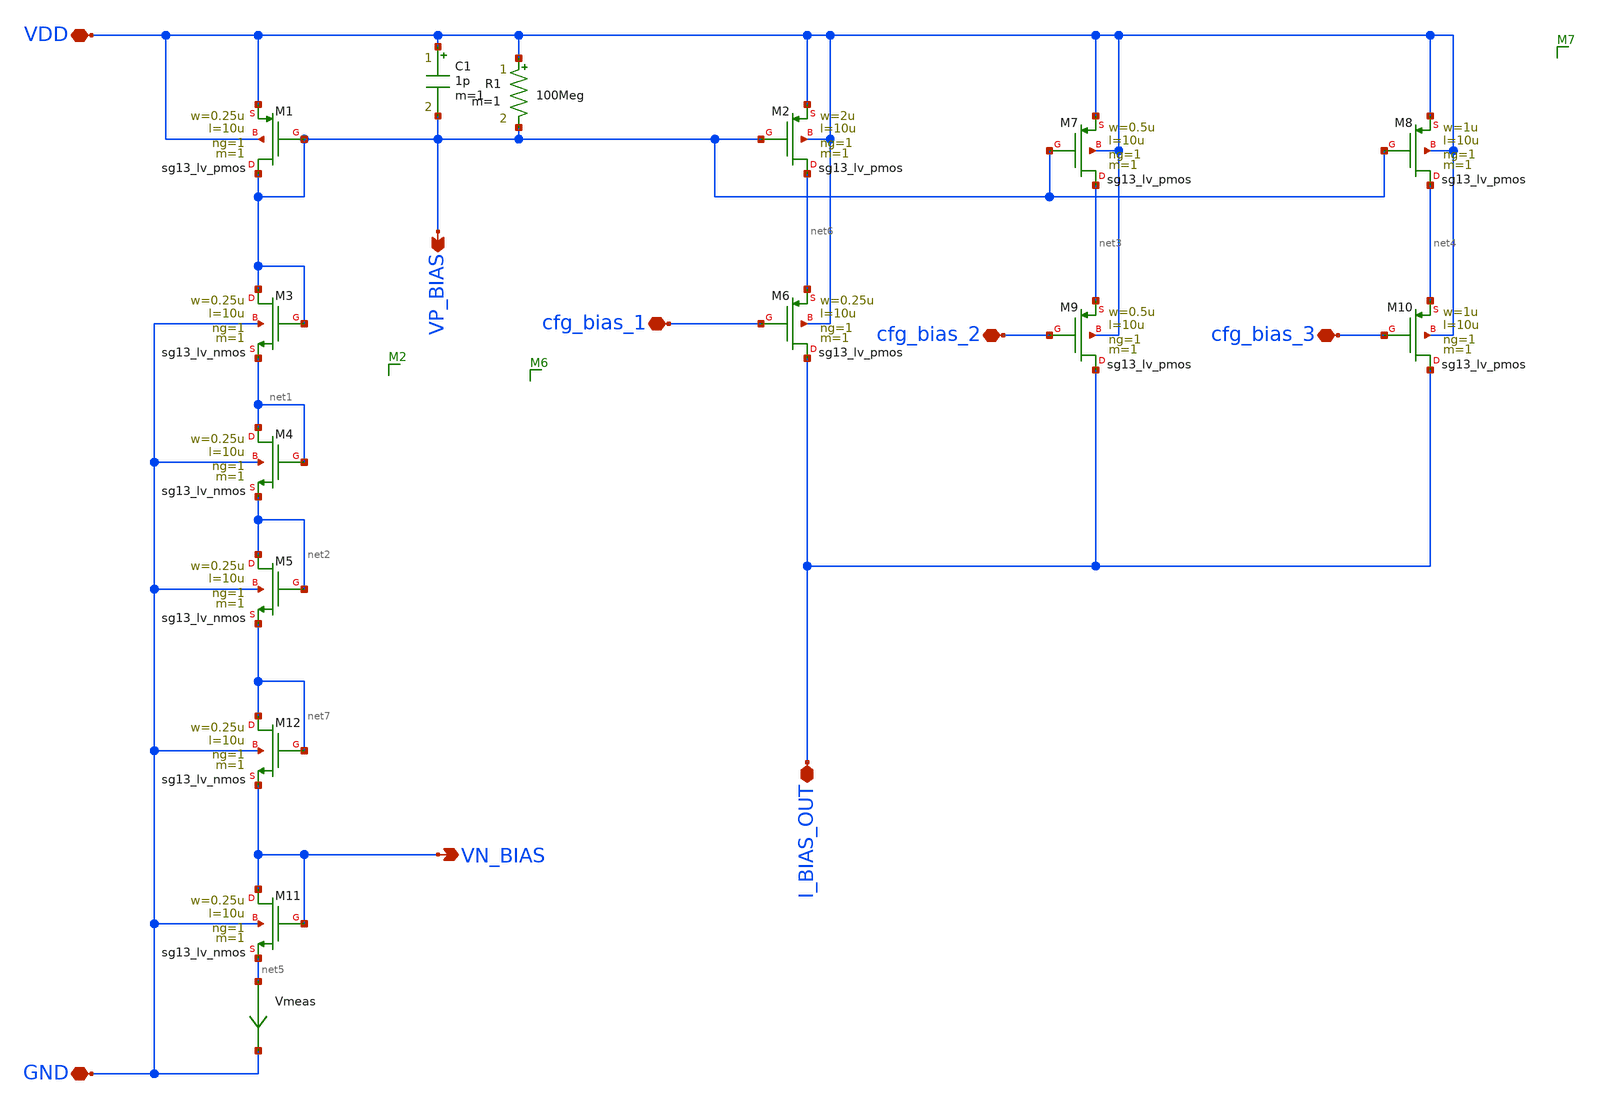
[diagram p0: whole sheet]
** sch_path: osc_bias.sch
**.subckt osc_bias VDD GND I_BIAS_OUT cfg_bias_1 cfg_bias_2 cfg_bias_3 VN_BIAS VP_BIAS
*.iopin VDD
*.iopin GND
*.iopin I_BIAS_OUT
*.iopin cfg_bias_1
*.iopin cfg_bias_2
*.iopin cfg_bias_3
*.opin VN_BIAS
*.opin VP_BIAS
XM1 VP_BIAS VP_BIAS VDD VDD sg13_lv_pmos w=0.25u l=10u ng=1 m=1 mm_ok=1
XM3 VP_BIAS VP_BIAS net1 GND sg13_lv_nmos w=0.25u l=10u ng=1 m=1 mm_ok=1
XM4 net1 net1 net2 GND sg13_lv_nmos w=0.25u l=10u ng=1 m=1 mm_ok=1
XM5 net2 net2 net7 GND sg13_lv_nmos w=0.25u l=10u ng=1 m=1 mm_ok=1
XM2 net6 VP_BIAS VDD VDD sg13_lv_pmos w=2u l=10u ng=1 m=1 mm_ok=1
XM6 I_BIAS_OUT cfg_bias_1 net6 VDD sg13_lv_pmos w=0.25u l=10u ng=1 m=1 mm_ok=1
XM7 net3 VP_BIAS VDD VDD sg13_lv_pmos w=0.5u l=10u ng=1 m=1 mm_ok=1
XM8 net4 VP_BIAS VDD VDD sg13_lv_pmos w=1u l=10u ng=1 m=1 mm_ok=1
XM9 I_BIAS_OUT cfg_bias_2 net3 VDD sg13_lv_pmos w=0.5u l=10u ng=1 m=1 mm_ok=1
XM10 I_BIAS_OUT cfg_bias_3 net4 VDD sg13_lv_pmos w=1u l=10u ng=1 m=1 mm_ok=1
XM11 VN_BIAS VN_BIAS net5 GND sg13_lv_nmos w=0.25u l=10u ng=1 m=1 mm_ok=1
Vmeas net5 GND 0
.save i(vmeas)
C1 VDD VP_BIAS 1p m=1
R1 VDD VP_BIAS 100Meg m=1
XM12 net7 net7 VN_BIAS GND sg13_lv_nmos w=0.25u l=10u ng=1 m=1 mm_ok=1
**.ends
.end
